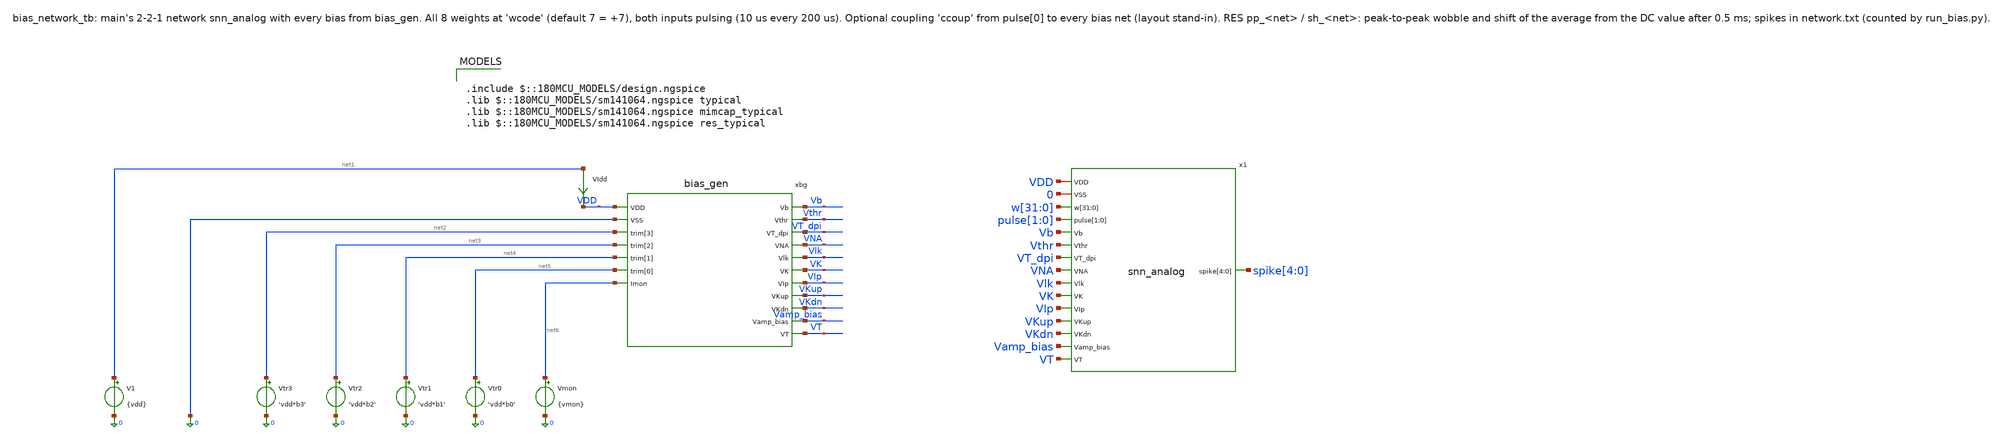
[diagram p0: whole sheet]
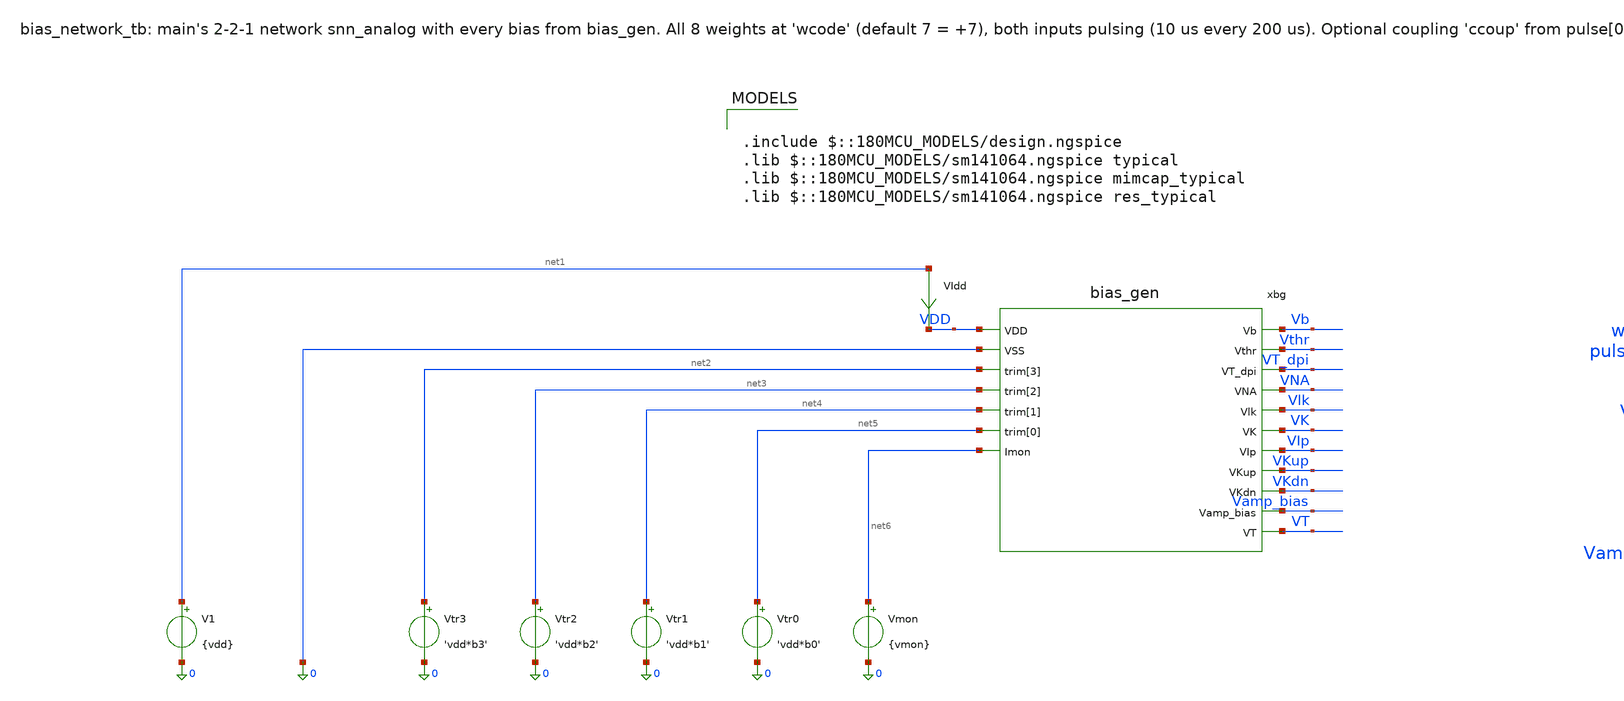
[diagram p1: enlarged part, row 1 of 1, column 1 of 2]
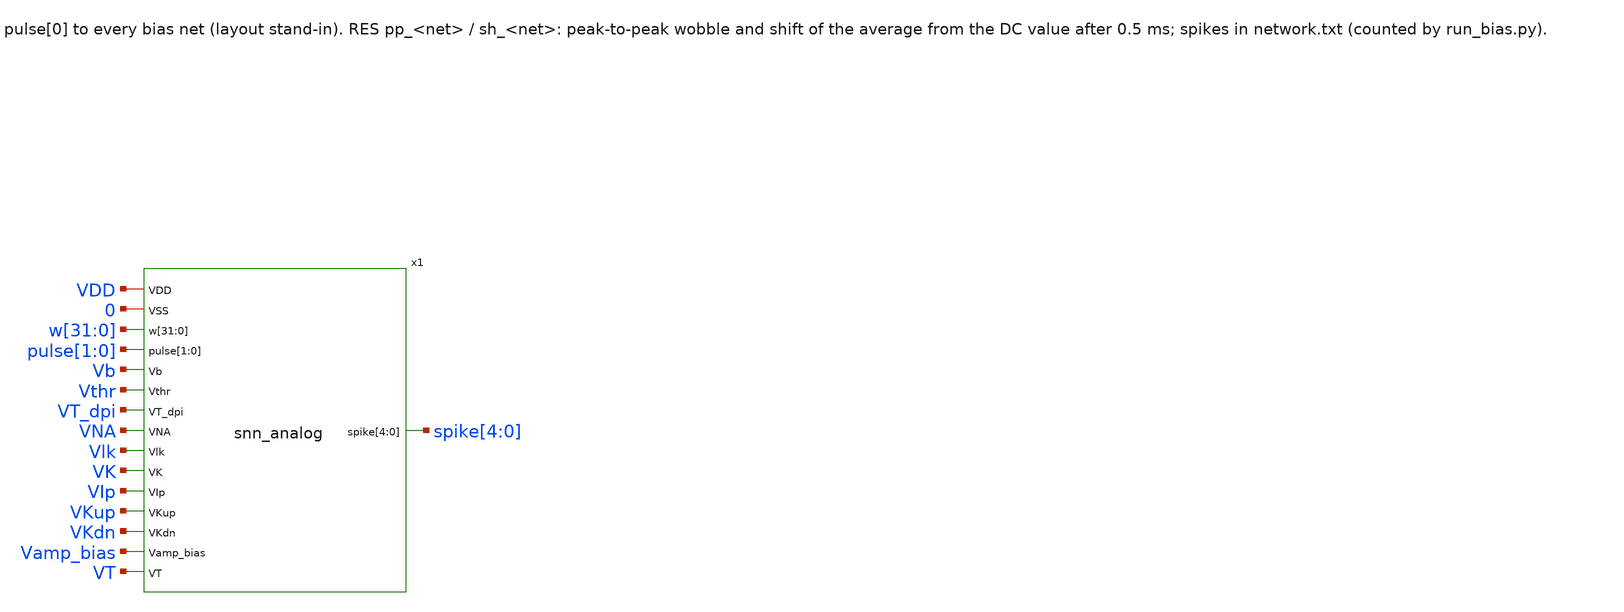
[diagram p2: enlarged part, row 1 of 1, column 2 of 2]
** sch_path: analog/bias/testbenches/bias_network_tb.sch
**.subckt bias_network_tb
xbg VDD 0 net2 net3 net4 net5 net6 Vb Vthr VT_dpi VNA Vlk VK VIp VKup VKdn Vamp_bias VT bias_gen
V1 net1 0 {vdd}
VIdd net1 VDD 0
.save i(vidd)
Vtr3 net2 0 'vdd*b3'
Vtr2 net3 0 'vdd*b2'
Vtr1 net4 0 'vdd*b1'
Vtr0 net5 0 'vdd*b0'
Vmon net6 0 {vmon}
x1 VDD 0 w[31] w[30] w[29] w[28] w[27] w[26] w[25] w[24] w[23] w[22] w[21] w[20] w[19] w[18] w[17]
+ w[16] w[15] w[14] w[13] w[12] w[11] w[10] w[9] w[8] w[7] w[6] w[5] w[4] w[3] w[2] w[1] w[0] pulse[1]
+ pulse[0] Vb Vthr VT_dpi VNA Vlk VK VIp VKup VKdn Vamp_bias VT spike[4] spike[3] spike[2] spike[1] spike[0]
+ snn_analog
**** begin user architecture code

.include $::180MCU_MODELS/design.ngspice
.lib $::180MCU_MODELS/sm141064.ngspice typical
.lib $::180MCU_MODELS/sm141064.ngspice mimcap_typical
.lib $::180MCU_MODELS/sm141064.ngspice res_typical



* weights: every 4-bit word = wcode (bit k = wk); inputs: 10 us pulses every 200 us
.param w3='floor(wcode/8)-2*floor(wcode/16)' w2='floor(wcode/4)-2*floor(wcode/8)'
.param w1='floor(wcode/2)-2*floor(wcode/4)' w0='wcode-2*floor(wcode/2)'
Vw0 w[0] 0 'vdd*w0'
Vw1 w[1] 0 'vdd*w1'
Vw2 w[2] 0 'vdd*w2'
Vw3 w[3] 0 'vdd*w3'
Vw4 w[4] 0 'vdd*w0'
Vw5 w[5] 0 'vdd*w1'
Vw6 w[6] 0 'vdd*w2'
Vw7 w[7] 0 'vdd*w3'
Vw8 w[8] 0 'vdd*w0'
Vw9 w[9] 0 'vdd*w1'
Vw10 w[10] 0 'vdd*w2'
Vw11 w[11] 0 'vdd*w3'
Vw12 w[12] 0 'vdd*w0'
Vw13 w[13] 0 'vdd*w1'
Vw14 w[14] 0 'vdd*w2'
Vw15 w[15] 0 'vdd*w3'
Vw16 w[16] 0 'vdd*w0'
Vw17 w[17] 0 'vdd*w1'
Vw18 w[18] 0 'vdd*w2'
Vw19 w[19] 0 'vdd*w3'
Vw20 w[20] 0 'vdd*w0'
Vw21 w[21] 0 'vdd*w1'
Vw22 w[22] 0 'vdd*w2'
Vw23 w[23] 0 'vdd*w3'
Vw24 w[24] 0 'vdd*w0'
Vw25 w[25] 0 'vdd*w1'
Vw26 w[26] 0 'vdd*w2'
Vw27 w[27] 0 'vdd*w3'
Vw28 w[28] 0 'vdd*w0'
Vw29 w[29] 0 'vdd*w1'
Vw30 w[30] 0 'vdd*w2'
Vw31 w[31] 0 'vdd*w3'
Vp0 pulse[0] 0 pulse(0 3.3 100u 10n 10n 10u 200u)
Vp1 pulse[1] 0 pulse(0 3.3 100u 10n 10n 10u 200u)
Cc_Vb pulse[0] Vb {ccoup}
Cc_Vthr pulse[0] Vthr {ccoup}
Cc_VT_dpi pulse[0] VT_dpi {ccoup}
Cc_VNA pulse[0] VNA {ccoup}
Cc_Vlk pulse[0] Vlk {ccoup}
Cc_VK pulse[0] VK {ccoup}
Cc_VIp pulse[0] VIp {ccoup}
Cc_VKup pulse[0] VKup {ccoup}
Cc_VKdn pulse[0] VKdn {ccoup}
Cc_Vamp_bias pulse[0] Vamp_bias {ccoup}
Cc_VT pulse[0] VT {ccoup}
Esp0 sp0 0 spike[0] 0 1
Esp1 sp1 0 spike[1] 0 1
Esp2 sp2 0 spike[2] 0 1
Esp3 sp3 0 spike[3] 0 1
Esp4 sp4 0 spike[4] 0 1
.ic v(x1.VMEM_0)=0 v(x1.VMEM_1)=0 v(x1.VMEM_2)=0 v(x1.VMEM_3)=0 v(x1.VMEM_4)=0 v(spike[0])=0
+ v(spike[1])=0 v(spike[2])=0 v(spike[3])=0 v(spike[4])=0




.param vdd=3.3 code=9 vmon=1.65
* trim bits of 'code' (b3 = MSB), driven by Vtr3..Vtr0
.param b3='floor(code/8)-2*floor(code/16)' b2='floor(code/4)-2*floor(code/8)'
.param b1='floor(code/2)-2*floor(code/4)' b0='code-2*floor(code/2)'
.csparam code_c={code}
.csparam vdd_c={vdd}
.param wcode=7 ccoup=0 tstop=3m
.csparam tstop_c={tstop}
.options method=gear
.control
  save v(sp0) v(sp1) v(sp2) v(sp3) v(sp4) v(Vb) v(Vthr) v(VT_dpi) v(VNA) v(Vlk) v(VK) v(VIp) v(VKup)
+ v(VKdn) v(Vamp_bias) v(VT)
  set wr_singlescale
  set wr_vecnames
  tran 0.1u $&tstop_c 0 0.1u
  meas tran hi_0 max v(Vb) from=0.5m
  meas tran lo_0 min v(Vb) from=0.5m
  meas tran av_0 avg v(Vb) from=0.5m
  let v0_0 = v(Vb)[0]
  let pp_0 = hi_0 - lo_0
  let sh_0 = av_0 - v0_0
  echo RES pp_Vb=$&pp_0
  echo RES sh_Vb=$&sh_0
  meas tran hi_1 max v(Vthr) from=0.5m
  meas tran lo_1 min v(Vthr) from=0.5m
  meas tran av_1 avg v(Vthr) from=0.5m
  let v0_1 = v(Vthr)[0]
  let pp_1 = hi_1 - lo_1
  let sh_1 = av_1 - v0_1
  echo RES pp_Vthr=$&pp_1
  echo RES sh_Vthr=$&sh_1
  meas tran hi_2 max v(VT_dpi) from=0.5m
  meas tran lo_2 min v(VT_dpi) from=0.5m
  meas tran av_2 avg v(VT_dpi) from=0.5m
  let v0_2 = v(VT_dpi)[0]
  let pp_2 = hi_2 - lo_2
  let sh_2 = av_2 - v0_2
  echo RES pp_VT_dpi=$&pp_2
  echo RES sh_VT_dpi=$&sh_2
  meas tran hi_3 max v(VNA) from=0.5m
  meas tran lo_3 min v(VNA) from=0.5m
  meas tran av_3 avg v(VNA) from=0.5m
  let v0_3 = v(VNA)[0]
  let pp_3 = hi_3 - lo_3
  let sh_3 = av_3 - v0_3
  echo RES pp_VNA=$&pp_3
  echo RES sh_VNA=$&sh_3
  meas tran hi_4 max v(Vlk) from=0.5m
  meas tran lo_4 min v(Vlk) from=0.5m
  meas tran av_4 avg v(Vlk) from=0.5m
  let v0_4 = v(Vlk)[0]
  let pp_4 = hi_4 - lo_4
  let sh_4 = av_4 - v0_4
  echo RES pp_Vlk=$&pp_4
  echo RES sh_Vlk=$&sh_4
  meas tran hi_5 max v(VK) from=0.5m
  meas tran lo_5 min v(VK) from=0.5m
  meas tran av_5 avg v(VK) from=0.5m
  let v0_5 = v(VK)[0]
  let pp_5 = hi_5 - lo_5
  let sh_5 = av_5 - v0_5
  echo RES pp_VK=$&pp_5
  echo RES sh_VK=$&sh_5
  meas tran hi_6 max v(VIp) from=0.5m
  meas tran lo_6 min v(VIp) from=0.5m
  meas tran av_6 avg v(VIp) from=0.5m
  let v0_6 = v(VIp)[0]
  let pp_6 = hi_6 - lo_6
  let sh_6 = av_6 - v0_6
  echo RES pp_VIp=$&pp_6
  echo RES sh_VIp=$&sh_6
  meas tran hi_7 max v(VKup) from=0.5m
  meas tran lo_7 min v(VKup) from=0.5m
  meas tran av_7 avg v(VKup) from=0.5m
  let v0_7 = v(VKup)[0]
  let pp_7 = hi_7 - lo_7
  let sh_7 = av_7 - v0_7
  echo RES pp_VKup=$&pp_7
  echo RES sh_VKup=$&sh_7
  meas tran hi_8 max v(VKdn) from=0.5m
  meas tran lo_8 min v(VKdn) from=0.5m
  meas tran av_8 avg v(VKdn) from=0.5m
  let v0_8 = v(VKdn)[0]
  let pp_8 = hi_8 - lo_8
  let sh_8 = av_8 - v0_8
  echo RES pp_VKdn=$&pp_8
  echo RES sh_VKdn=$&sh_8
  meas tran hi_9 max v(Vamp_bias) from=0.5m
  meas tran lo_9 min v(Vamp_bias) from=0.5m
  meas tran av_9 avg v(Vamp_bias) from=0.5m
  let v0_9 = v(Vamp_bias)[0]
  let pp_9 = hi_9 - lo_9
  let sh_9 = av_9 - v0_9
  echo RES pp_Vamp_bias=$&pp_9
  echo RES sh_Vamp_bias=$&sh_9
  meas tran hi_10 max v(VT) from=0.5m
  meas tran lo_10 min v(VT) from=0.5m
  meas tran av_10 avg v(VT) from=0.5m
  let v0_10 = v(VT)[0]
  let pp_10 = hi_10 - lo_10
  let sh_10 = av_10 - v0_10
  echo RES pp_VT=$&pp_10
  echo RES sh_VT=$&sh_10
  wrdata network.txt v(sp0) v(sp1) v(sp2) v(sp3) v(sp4)
  if $?batchmode = 0
    plot v(sp4)+4 v(sp3) v(Vthr) v(VT_dpi) title 'output, hid1 spikes; DPI biases'
  end
.endc


**** end user architecture code
**.ends
.end
